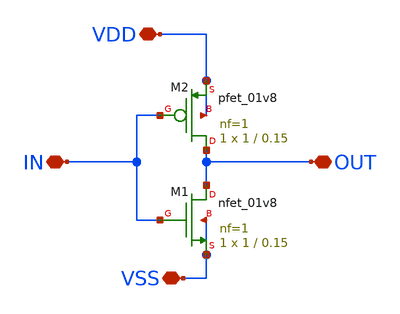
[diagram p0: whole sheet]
** sch_path: inverter/inverter.sch
**.subckt inverter IN VDD VSS OUT
*.iopin IN
*.iopin VDD
*.iopin VSS
*.iopin OUT
XM1 OUT IN VSS VSS sky130_fd_pr__nfet_01v8 L=0.15 W=1 nf=1 ad='int((nf+1)/2) * W/nf * 0.29' as='int((nf+2)/2) * W/nf * 0.29'
+ pd='2*int((nf+1)/2) * (W/nf + 0.29)' ps='2*int((nf+2)/2) * (W/nf + 0.29)' nrd='0.29 / W' nrs='0.29 / W'
+ sa=0 sb=0 sd=0 mult=1 m=1
XM2 OUT IN VDD VDD sky130_fd_pr__pfet_01v8 L=0.15 W=1 nf=1 ad='int((nf+1)/2) * W/nf * 0.29' as='int((nf+2)/2) * W/nf * 0.29'
+ pd='2*int((nf+1)/2) * (W/nf + 0.29)' ps='2*int((nf+2)/2) * (W/nf + 0.29)' nrd='0.29 / W' nrs='0.29 / W'
+ sa=0 sb=0 sd=0 mult=1 m=1
**** begin user architecture code


.lib /foss/pdks/sky130A/libs.tech/ngspice/sky130.lib.spice tt



**** end user architecture code
**.ends
.end
